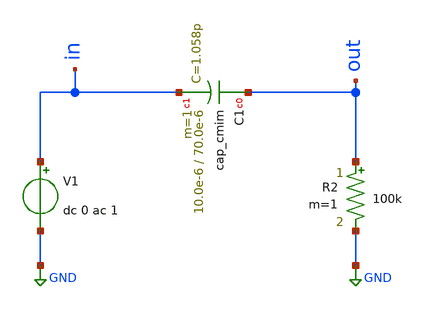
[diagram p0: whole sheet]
** sch_path: ihp-sg13g2/xschem_libs/sg13g2_tests_ase/ac_mim_cap/schematic/ac_mim_cap.sch
* Copyright 2021 Stefan Frederik Schippers
* Licensed under the Apache License, Version 2.0 (the "License");
* you may not use this file except in compliance with the License.
* You may obtain a copy of the License at
* https://www.apache.org/licenses/LICENSE-2.0
* Unless required by applicable law or agreed to in writing, software
* distributed under the License is distributed on an "AS IS" BASIS,
* WITHOUT WARRANTIES OR CONDITIONS OF ANY KIND, either express or implied.
* See the License for the specific language governing permissions and
* limitations under the License.
* Copyright 2023 IHP PDK Authors
**.subckt ac_mim_cap
V1 in GND dc 0 ac 1
R2 out GND 100k m=1
XC1 out in cap_cmim w=10.0e-6 l=70.0e-6 m=1 mm_ok=1
**.ends
.GLOBAL GND
.end
